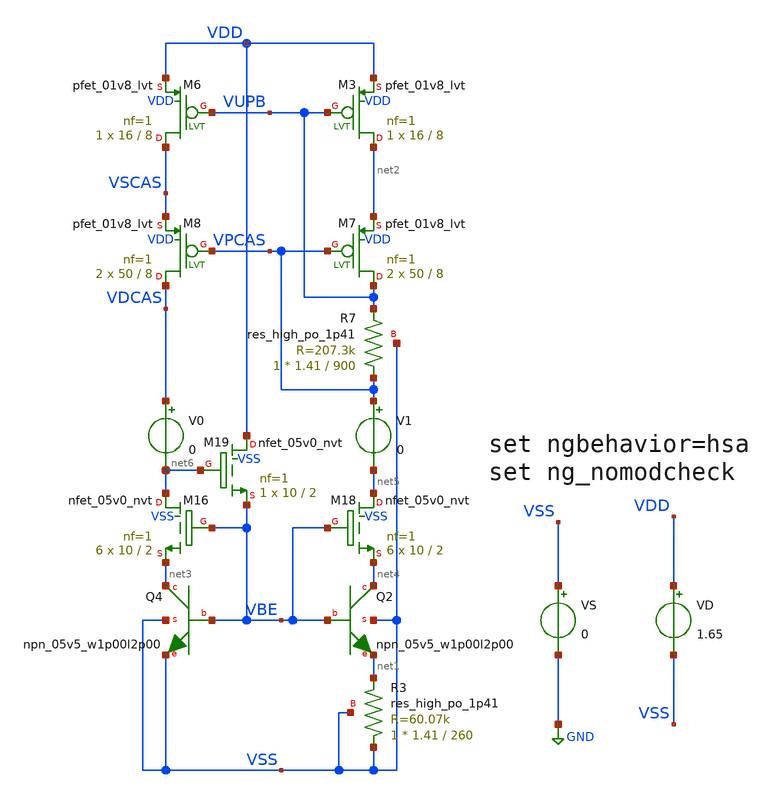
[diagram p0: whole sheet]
** sch_path: testbenches/temp_char_ptat_ctat.sch
**.subckt temp_char_ptat_ctat
VD VDD VSS 1.65
.save i(vd)
VS VSS GND 0
V0 VDCAS net6 0
.save i(v0)
V1 VPCAS net5 0
.save i(v1)
XM3 net2 VUPB VDD VDD sky130_fd_pr__pfet_01v8_lvt L=8 W=16 nf=1 ad='int((nf+1)/2) * W/nf * 0.29' as='int((nf+2)/2) * W/nf * 0.29'
+ pd='2*int((nf+1)/2) * (W/nf + 0.29)' ps='2*int((nf+2)/2) * (W/nf + 0.29)' nrd='0.29 / W' nrs='0.29 / W'
+ sa=0 sb=0 sd=0 mult=1 m=1
XM6 VSCAS VUPB VDD VDD sky130_fd_pr__pfet_01v8_lvt L=8 W=16 nf=1 ad='int((nf+1)/2) * W/nf * 0.29' as='int((nf+2)/2) * W/nf * 0.29'
+ pd='2*int((nf+1)/2) * (W/nf + 0.29)' ps='2*int((nf+2)/2) * (W/nf + 0.29)' nrd='0.29 / W' nrs='0.29 / W'
+ sa=0 sb=0 sd=0 mult=1 m=1
XQ2 net4 VBE net1 VSS sky130_fd_pr__npn_05v5_w1p00l2p00
XQ4 net3 VBE VSS VSS sky130_fd_pr__npn_05v5_w1p00l2p00
XR3 VSS net1 VSS sky130_fd_pr__res_high_po_1p41 L=260 mult=1 m=1
XM7 VUPB VPCAS net2 VDD sky130_fd_pr__pfet_01v8_lvt L=8 W=50 nf=1 ad='int((nf+1)/2) * W/nf * 0.29' as='int((nf+2)/2) * W/nf * 0.29'
+ pd='2*int((nf+1)/2) * (W/nf + 0.29)' ps='2*int((nf+2)/2) * (W/nf + 0.29)' nrd='0.29 / W' nrs='0.29 / W'
+ sa=0 sb=0 sd=0 mult=2 m=2
XM8 VDCAS VPCAS VSCAS VDD sky130_fd_pr__pfet_01v8_lvt L=8 W=50 nf=1 ad='int((nf+1)/2) * W/nf * 0.29'
+ as='int((nf+2)/2) * W/nf * 0.29' pd='2*int((nf+1)/2) * (W/nf + 0.29)' ps='2*int((nf+2)/2) * (W/nf + 0.29)'
+ nrd='0.29 / W' nrs='0.29 / W' sa=0 sb=0 sd=0 mult=2 m=2
XR7 VPCAS VUPB VSS sky130_fd_pr__res_high_po_1p41 L=900 mult=1 m=1
XM16 net6 VBE net3 VSS sky130_fd_pr__nfet_05v0_nvt L=2 W=10 nf=1 ad='int((nf+1)/2) * W/nf * 0.29' as='int((nf+2)/2) * W/nf * 0.29'
+ pd='2*int((nf+1)/2) * (W/nf + 0.29)' ps='2*int((nf+2)/2) * (W/nf + 0.29)' nrd='0.29 / W' nrs='0.29 / W'
+ sa=0 sb=0 sd=0 mult=6 m=6
XM18 net5 VBE net4 VSS sky130_fd_pr__nfet_05v0_nvt L=2 W=10 nf=1 ad='int((nf+1)/2) * W/nf * 0.29' as='int((nf+2)/2) * W/nf * 0.29'
+ pd='2*int((nf+1)/2) * (W/nf + 0.29)' ps='2*int((nf+2)/2) * (W/nf + 0.29)' nrd='0.29 / W' nrs='0.29 / W'
+ sa=0 sb=0 sd=0 mult=6 m=6
XM19 VDD net6 VBE VSS sky130_fd_pr__nfet_05v0_nvt L=2 W=10 nf=1 ad='int((nf+1)/2) * W/nf * 0.29' as='int((nf+2)/2) * W/nf * 0.29'
+ pd='2*int((nf+1)/2) * (W/nf + 0.29)' ps='2*int((nf+2)/2) * (W/nf + 0.29)' nrd='0.29 / W' nrs='0.29 / W'
+ sa=0 sb=0 sd=0 mult=1 m=1
**** begin user architecture code


** Analysis Requests **
** Outputs Requests **
.option wnflag=1
.option savecurrents
.control
save all
dc temp -40 125 5
remzerovec
wrdata ~/.xschem/simulations/temp_char_ptat_ctat.txt i(V0) i(V1)/i(V0) v(VBE) v(VUPB)
*plot V(VBE), V(VUPB)
plot V(VSCAS) - V(VDCAS)
plot I(V1)/I(V0)
plot I(V0), I(V1)
set temp = 125
op
write ~/.xschem/simulations/temp_char_ptat_ctat.raw
.endc



** opencircuitdesign pdks install
.lib /foss/pdks/sky130A/libs.tech/combined/sky130.corners.lib.spice fshh

**** end user architecture code
**.ends
.GLOBAL GND
.end
